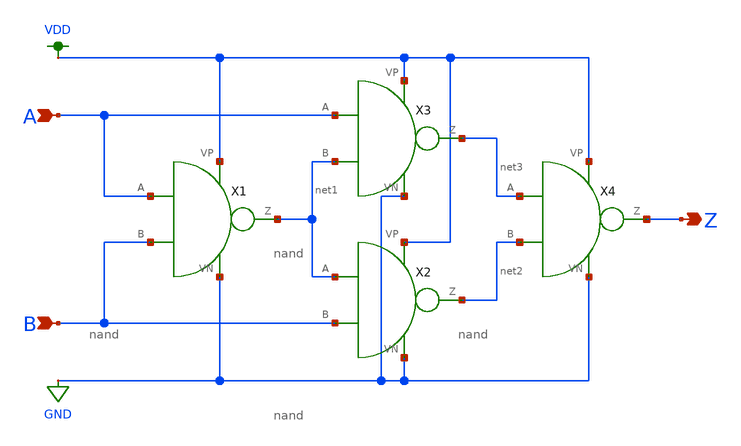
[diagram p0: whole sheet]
** sch_path: LVS/xor.sch
**.subckt xor A B Z
*.ipin A
*.ipin B
*.opin Z
X1 A B VDD GND net1 nand
X2 net1 B VDD GND net2 nand
X3 A net1 VDD GND net3 nand
X4 net3 net2 VDD GND Z nand
**.ends

* expanding   symbol:  /home/madvlsi/Documents/MADVLSI_final/schematics/nand.sym # of pins=6
** sym_path: schematics/nand.sym
** sch_path: schematics/nand.sch
.subckt nand A B VP VN Z
*.ipin A
*.iopin VP
*.iopin VN
*.opin Z
*.ipin B
XM1 Z A net1 GND sky130_fd_pr__nfet_01v8 L=0.15 W=1 nf=1 ad='int((nf+1)/2) * W/nf * 0.29' as='int((nf+2)/2) * W/nf * 0.29'
+ pd='2*int((nf+1)/2) * (W/nf + 0.29)' ps='2*int((nf+2)/2) * (W/nf + 0.29)' nrd='0.29 / W' nrs='0.29 / W'
+ sa=0 sb=0 sd=0 mult=1 m=1
XM2 VP B Z VDD sky130_fd_pr__pfet_01v8 L=0.15 W=1 nf=1 ad='int((nf+1)/2) * W/nf * 0.29' as='int((nf+2)/2) * W/nf * 0.29'
+ pd='2*int((nf+1)/2) * (W/nf + 0.29)' ps='2*int((nf+2)/2) * (W/nf + 0.29)' nrd='0.29 / W' nrs='0.29 / W'
+ sa=0 sb=0 sd=0 mult=2 m=2
XM3 VN B net1 GND sky130_fd_pr__nfet_01v8 L=0.15 W=1 nf=1 ad='int((nf+1)/2) * W/nf * 0.29' as='int((nf+2)/2) * W/nf * 0.29'
+ pd='2*int((nf+1)/2) * (W/nf + 0.29)' ps='2*int((nf+2)/2) * (W/nf + 0.29)' nrd='0.29 / W' nrs='0.29 / W'
+ sa=0 sb=0 sd=0 mult=1 m=1
XM4 Z A VP VDD sky130_fd_pr__pfet_01v8 L=0.15 W=1 nf=1 ad='int((nf+1)/2) * W/nf * 0.29' as='int((nf+2)/2) * W/nf * 0.29'
+ pd='2*int((nf+1)/2) * (W/nf + 0.29)' ps='2*int((nf+2)/2) * (W/nf + 0.29)' nrd='0.29 / W' nrs='0.29 / W'
+ sa=0 sb=0 sd=0 mult=2 m=2
.ends

.GLOBAL GND
.GLOBAL VDD
.end
